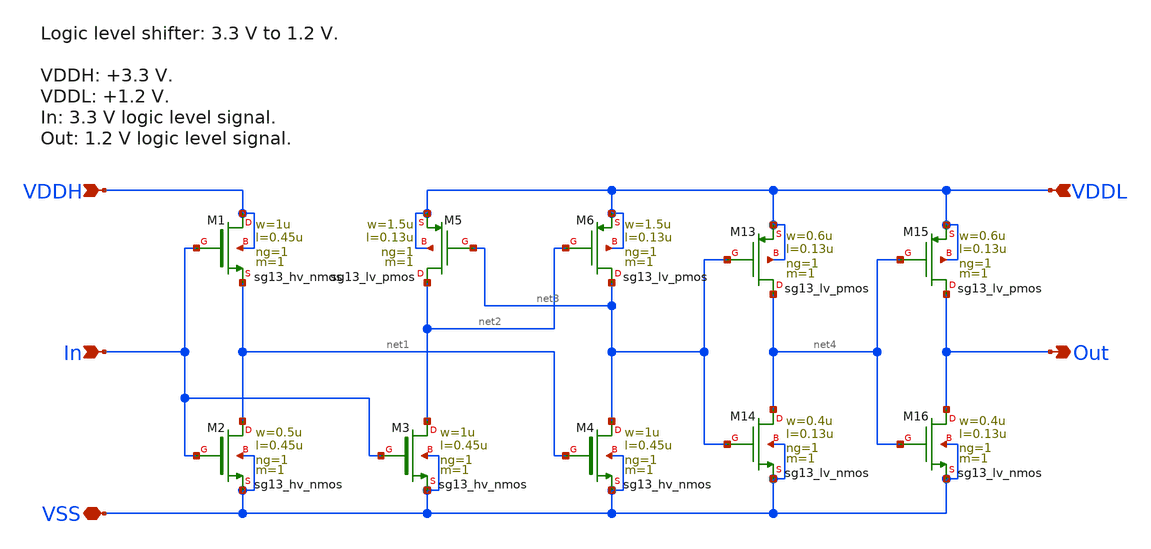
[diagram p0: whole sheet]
** sch_path: sar_adc/xschem/blocks/hv_lv_level_shifter/hv_lv_level_shifter.sch
**.subckt hv_lv_level_shifter VDDH In VSS VDDL Out
*.ipin VDDH
*.ipin In
*.iopin VSS
*.ipin VDDL
*.opin Out
XM1 VDDH In net1 VDDH sg13_hv_nmos w=1u l=0.45u ng=1 m=1 mm_ok=1
XM2 net1 In VSS VSS sg13_hv_nmos w=0.5u l=0.45u ng=1 m=1 mm_ok=1
XM3 net2 In VSS VSS sg13_hv_nmos w=1u l=0.45u ng=1 m=1 mm_ok=1
XM4 net3 net1 VSS VSS sg13_hv_nmos w=1u l=0.45u ng=1 m=1 mm_ok=1
XM5 net2 net3 VDDL VDDL sg13_lv_pmos w=1.5u l=0.13u ng=1 m=1 mm_ok=1
XM6 net3 net2 VDDL VDDL sg13_lv_pmos w=1.5u l=0.13u ng=1 m=1 mm_ok=1
XM13 net4 net3 VDDL VDDL sg13_lv_pmos w=0.6u l=0.13u ng=1 m=1 mm_ok=1
XM14 net4 net3 VSS VSS sg13_lv_nmos w=0.4u l=0.13u ng=1 m=1 mm_ok=1
XM15 Out net4 VDDL VDDL sg13_lv_pmos w=0.6u l=0.13u ng=1 m=1 mm_ok=1
XM16 Out net4 VSS VSS sg13_lv_nmos w=0.4u l=0.13u ng=1 m=1 mm_ok=1
**.ends
.end
